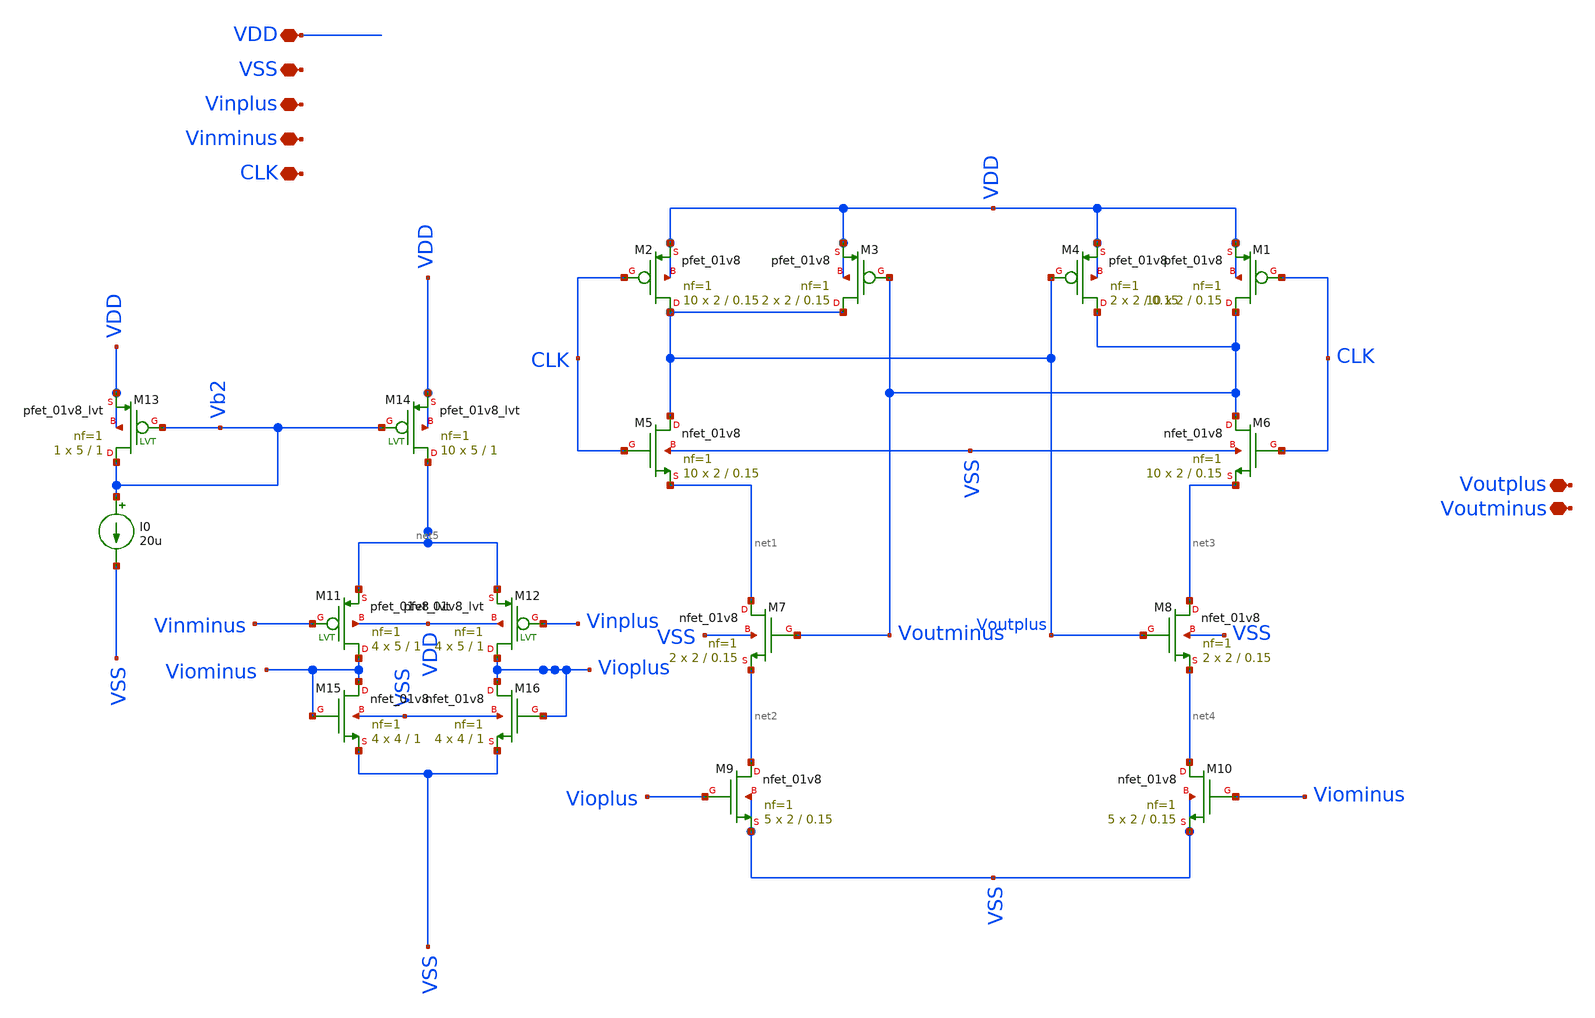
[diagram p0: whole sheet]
** sch_path: xschem/Amplifiers/Comparator.sch
**.subckt Comparator VDD VSS Vinplus Vinminus CLK Voutplus Voutminus
*.iopin VDD
*.iopin VSS
*.iopin Vinplus
*.iopin Vinminus
*.iopin CLK
*.iopin Voutplus
*.iopin Voutminus
XM3 Voutplus Voutminus VDD VDD sky130_fd_pr__pfet_01v8 L=0.15 W=2 nf=1 ad='int((nf+1)/2) * W/nf * 0.29'
+ as='int((nf+2)/2) * W/nf * 0.29' pd='2*int((nf+1)/2) * (W/nf + 0.29)' ps='2*int((nf+2)/2) * (W/nf + 0.29)'
+ nrd='0.29 / W' nrs='0.29 / W' sa=0 sb=0 sd=0 mult=2 m=2
XM4 Voutminus Voutplus VDD VDD sky130_fd_pr__pfet_01v8 L=0.15 W=2 nf=1 ad='int((nf+1)/2) * W/nf * 0.29'
+ as='int((nf+2)/2) * W/nf * 0.29' pd='2*int((nf+1)/2) * (W/nf + 0.29)' ps='2*int((nf+2)/2) * (W/nf + 0.29)'
+ nrd='0.29 / W' nrs='0.29 / W' sa=0 sb=0 sd=0 mult=2 m=2
XM5 Voutplus CLK net1 VSS sky130_fd_pr__nfet_01v8 L=0.15 W=2 nf=1 ad='int((nf+1)/2) * W/nf * 0.29' as='int((nf+2)/2) * W/nf * 0.29'
+ pd='2*int((nf+1)/2) * (W/nf + 0.29)' ps='2*int((nf+2)/2) * (W/nf + 0.29)' nrd='0.29 / W' nrs='0.29 / W'
+ sa=0 sb=0 sd=0 mult=10 m=10
XM6 Voutminus CLK net3 VSS sky130_fd_pr__nfet_01v8 L=0.15 W=2 nf=1 ad='int((nf+1)/2) * W/nf * 0.29' as='int((nf+2)/2) * W/nf * 0.29'
+ pd='2*int((nf+1)/2) * (W/nf + 0.29)' ps='2*int((nf+2)/2) * (W/nf + 0.29)' nrd='0.29 / W' nrs='0.29 / W'
+ sa=0 sb=0 sd=0 mult=10 m=10
XM7 net1 Voutminus net2 VSS sky130_fd_pr__nfet_01v8 L=0.15 W=2 nf=1 ad='int((nf+1)/2) * W/nf * 0.29'
+ as='int((nf+2)/2) * W/nf * 0.29' pd='2*int((nf+1)/2) * (W/nf + 0.29)' ps='2*int((nf+2)/2) * (W/nf + 0.29)'
+ nrd='0.29 / W' nrs='0.29 / W' sa=0 sb=0 sd=0 mult=2 m=2
XM8 net3 Voutplus net4 VSS sky130_fd_pr__nfet_01v8 L=0.15 W=2 nf=1 ad='int((nf+1)/2) * W/nf * 0.29' as='int((nf+2)/2) * W/nf * 0.29'
+ pd='2*int((nf+1)/2) * (W/nf + 0.29)' ps='2*int((nf+2)/2) * (W/nf + 0.29)' nrd='0.29 / W' nrs='0.29 / W'
+ sa=0 sb=0 sd=0 mult=2 m=2
XM9 net2 Vioplus VSS VSS sky130_fd_pr__nfet_01v8 L=0.15 W=2 nf=1 ad='int((nf+1)/2) * W/nf * 0.29' as='int((nf+2)/2) * W/nf * 0.29'
+ pd='2*int((nf+1)/2) * (W/nf + 0.29)' ps='2*int((nf+2)/2) * (W/nf + 0.29)' nrd='0.29 / W' nrs='0.29 / W'
+ sa=0 sb=0 sd=0 mult=5 m=5
XM10 net4 Viominus VSS VSS sky130_fd_pr__nfet_01v8 L=0.15 W=2 nf=1 ad='int((nf+1)/2) * W/nf * 0.29' as='int((nf+2)/2) * W/nf * 0.29'
+ pd='2*int((nf+1)/2) * (W/nf + 0.29)' ps='2*int((nf+2)/2) * (W/nf + 0.29)' nrd='0.29 / W' nrs='0.29 / W'
+ sa=0 sb=0 sd=0 mult=5 m=5
XM1 Voutminus CLK VDD VDD sky130_fd_pr__pfet_01v8 L=0.15 W=2 nf=1 ad='int((nf+1)/2) * W/nf * 0.29' as='int((nf+2)/2) * W/nf * 0.29'
+ pd='2*int((nf+1)/2) * (W/nf + 0.29)' ps='2*int((nf+2)/2) * (W/nf + 0.29)' nrd='0.29 / W' nrs='0.29 / W'
+ sa=0 sb=0 sd=0 mult=10 m=10
XM2 Voutplus CLK VDD VDD sky130_fd_pr__pfet_01v8 L=0.15 W=2 nf=1 ad='int((nf+1)/2) * W/nf * 0.29' as='int((nf+2)/2) * W/nf * 0.29'
+ pd='2*int((nf+1)/2) * (W/nf + 0.29)' ps='2*int((nf+2)/2) * (W/nf + 0.29)' nrd='0.29 / W' nrs='0.29 / W'
+ sa=0 sb=0 sd=0 mult=10 m=10
I0 Vb2 VSS 20u
XM11 Viominus Vinminus net5 VDD sky130_fd_pr__pfet_01v8_lvt L=1 W=5 nf=1 ad='int((nf+1)/2) * W/nf * 0.29'
+ as='int((nf+2)/2) * W/nf * 0.29' pd='2*int((nf+1)/2) * (W/nf + 0.29)' ps='2*int((nf+2)/2) * (W/nf + 0.29)'
+ nrd='0.29 / W' nrs='0.29 / W' sa=0 sb=0 sd=0 mult=4 m=4
XM12 Vioplus Vinplus net5 VDD sky130_fd_pr__pfet_01v8_lvt L=1 W=5 nf=1 ad='int((nf+1)/2) * W/nf * 0.29'
+ as='int((nf+2)/2) * W/nf * 0.29' pd='2*int((nf+1)/2) * (W/nf + 0.29)' ps='2*int((nf+2)/2) * (W/nf + 0.29)'
+ nrd='0.29 / W' nrs='0.29 / W' sa=0 sb=0 sd=0 mult=4 m=4
XM13 Vb2 Vb2 VDD VDD sky130_fd_pr__pfet_01v8_lvt L=1 W=5 nf=1 ad='int((nf+1)/2) * W/nf * 0.29' as='int((nf+2)/2) * W/nf * 0.29'
+ pd='2*int((nf+1)/2) * (W/nf + 0.29)' ps='2*int((nf+2)/2) * (W/nf + 0.29)' nrd='0.29 / W' nrs='0.29 / W'
+ sa=0 sb=0 sd=0 mult=1 m=1
XM14 net5 Vb2 VDD VDD sky130_fd_pr__pfet_01v8_lvt L=1 W=5 nf=1 ad='int((nf+1)/2) * W/nf * 0.29' as='int((nf+2)/2) * W/nf * 0.29'
+ pd='2*int((nf+1)/2) * (W/nf + 0.29)' ps='2*int((nf+2)/2) * (W/nf + 0.29)' nrd='0.29 / W' nrs='0.29 / W'
+ sa=0 sb=0 sd=0 mult=10 m=10
XM15 Viominus Viominus VSS VSS sky130_fd_pr__nfet_01v8 L=1 W=4 nf=1 ad='int((nf+1)/2) * W/nf * 0.29'
+ as='int((nf+2)/2) * W/nf * 0.29' pd='2*int((nf+1)/2) * (W/nf + 0.29)' ps='2*int((nf+2)/2) * (W/nf + 0.29)'
+ nrd='0.29 / W' nrs='0.29 / W' sa=0 sb=0 sd=0 mult=4 m=4
XM16 Vioplus Vioplus VSS VSS sky130_fd_pr__nfet_01v8 L=1 W=4 nf=1 ad='int((nf+1)/2) * W/nf * 0.29' as='int((nf+2)/2) * W/nf * 0.29'
+ pd='2*int((nf+1)/2) * (W/nf + 0.29)' ps='2*int((nf+2)/2) * (W/nf + 0.29)' nrd='0.29 / W' nrs='0.29 / W'
+ sa=0 sb=0 sd=0 mult=4 m=4
**.ends
.end
